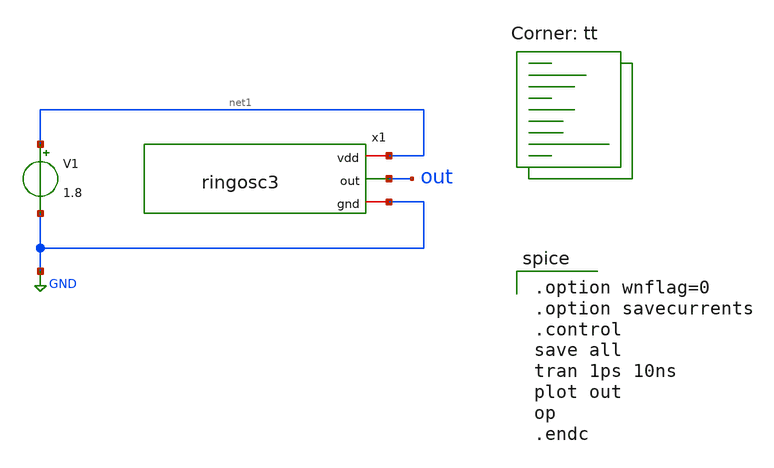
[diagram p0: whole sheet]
** sch_path: latiahan1/ringosc3_tb.sch
**.subckt ringosc3_tb
x1 net1 out GND ringosc3
V1 net1 GND 1.8
**** begin user architecture code

.option wnflag=0
.option savecurrents
.control
save all
tran 1ps 10ns
plot out
op
.endc


.lib $::SKYWATER_MODELS/sky130.lib.spice tt
**** end user architecture code
**.ends
.GLOBAL GND
.end
